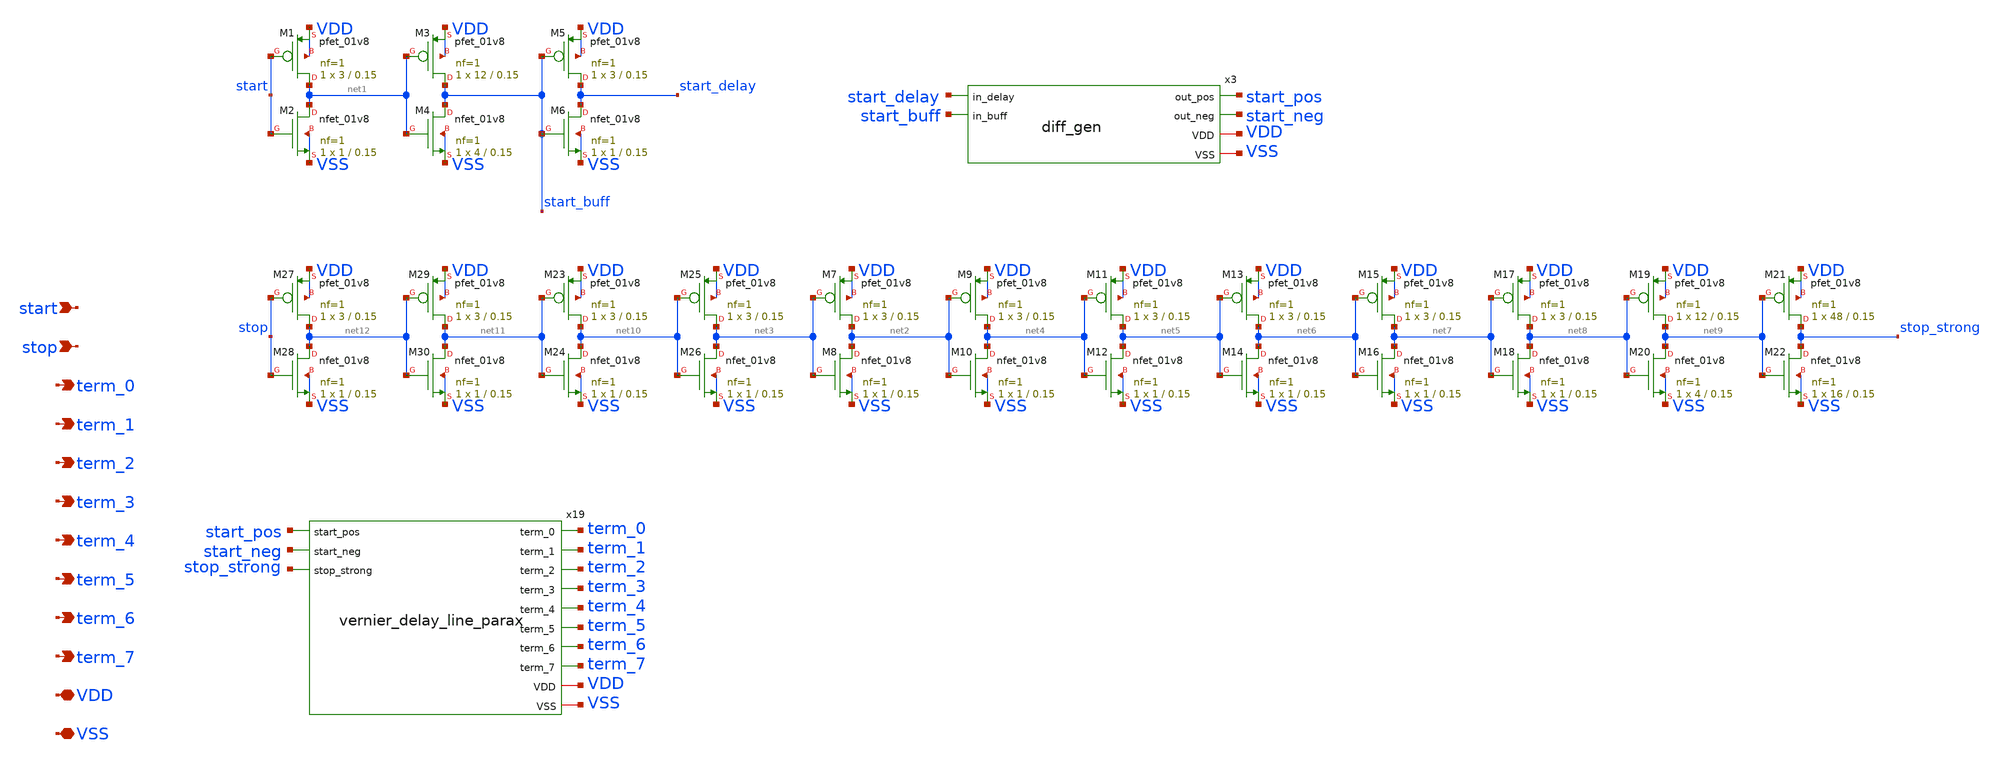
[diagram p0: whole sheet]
** sch_path: xschem/tdc_vernier_delay_line_post_layout.sch
**.subckt tdc_vernier_delay_line_post_layout VDD VSS start stop term_0 term_1 term_2 term_3 term_4
*+ term_5 term_6 term_7
*.iopin VDD
*.iopin VSS
*.ipin start
*.ipin stop
*.opin term_0
*.opin term_1
*.opin term_2
*.opin term_3
*.opin term_4
*.opin term_5
*.opin term_6
*.opin term_7
x3 start_delay start_buff start_pos start_neg VDD VSS diff_gen
XM1 net1 start VDD VDD sky130_fd_pr__pfet_01v8 L=0.15 W=3 nf=1 ad='int((nf+1)/2) * W/nf * 0.29' as='int((nf+2)/2) * W/nf * 0.29'
+ pd='2*int((nf+1)/2) * (W/nf + 0.29)' ps='2*int((nf+2)/2) * (W/nf + 0.29)' nrd='0.29 / W' nrs='0.29 / W'
+ sa=0 sb=0 sd=0 mult=1 m=1
XM2 net1 start VSS VSS sky130_fd_pr__nfet_01v8 L=0.15 W=1 nf=1 ad='int((nf+1)/2) * W/nf * 0.29' as='int((nf+2)/2) * W/nf * 0.29'
+ pd='2*int((nf+1)/2) * (W/nf + 0.29)' ps='2*int((nf+2)/2) * (W/nf + 0.29)' nrd='0.29 / W' nrs='0.29 / W'
+ sa=0 sb=0 sd=0 mult=1 m=1
XM3 start_buff net1 VDD VDD sky130_fd_pr__pfet_01v8 L=0.15 W=12 nf=1 ad='int((nf+1)/2) * W/nf * 0.29'
+ as='int((nf+2)/2) * W/nf * 0.29' pd='2*int((nf+1)/2) * (W/nf + 0.29)' ps='2*int((nf+2)/2) * (W/nf + 0.29)'
+ nrd='0.29 / W' nrs='0.29 / W' sa=0 sb=0 sd=0 mult=1 m=1
XM4 start_buff net1 VSS VSS sky130_fd_pr__nfet_01v8 L=0.15 W=4 nf=1 ad='int((nf+1)/2) * W/nf * 0.29'
+ as='int((nf+2)/2) * W/nf * 0.29' pd='2*int((nf+1)/2) * (W/nf + 0.29)' ps='2*int((nf+2)/2) * (W/nf + 0.29)'
+ nrd='0.29 / W' nrs='0.29 / W' sa=0 sb=0 sd=0 mult=1 m=1
XM5 start_delay start_buff VDD VDD sky130_fd_pr__pfet_01v8 L=0.15 W=3 nf=1 ad='int((nf+1)/2) * W/nf * 0.29'
+ as='int((nf+2)/2) * W/nf * 0.29' pd='2*int((nf+1)/2) * (W/nf + 0.29)' ps='2*int((nf+2)/2) * (W/nf + 0.29)'
+ nrd='0.29 / W' nrs='0.29 / W' sa=0 sb=0 sd=0 mult=1 m=1
XM6 start_delay start_buff VSS VSS sky130_fd_pr__nfet_01v8 L=0.15 W=1 nf=1 ad='int((nf+1)/2) * W/nf * 0.29'
+ as='int((nf+2)/2) * W/nf * 0.29' pd='2*int((nf+1)/2) * (W/nf + 0.29)' ps='2*int((nf+2)/2) * (W/nf + 0.29)'
+ nrd='0.29 / W' nrs='0.29 / W' sa=0 sb=0 sd=0 mult=1 m=1
XM7 net2 net3 VDD VDD sky130_fd_pr__pfet_01v8 L=0.15 W=3 nf=1 ad='int((nf+1)/2) * W/nf * 0.29' as='int((nf+2)/2) * W/nf * 0.29'
+ pd='2*int((nf+1)/2) * (W/nf + 0.29)' ps='2*int((nf+2)/2) * (W/nf + 0.29)' nrd='0.29 / W' nrs='0.29 / W'
+ sa=0 sb=0 sd=0 mult=1 m=1
XM8 net2 net3 VSS VSS sky130_fd_pr__nfet_01v8 L=0.15 W=1 nf=1 ad='int((nf+1)/2) * W/nf * 0.29' as='int((nf+2)/2) * W/nf * 0.29'
+ pd='2*int((nf+1)/2) * (W/nf + 0.29)' ps='2*int((nf+2)/2) * (W/nf + 0.29)' nrd='0.29 / W' nrs='0.29 / W'
+ sa=0 sb=0 sd=0 mult=1 m=1
XM9 net4 net2 VDD VDD sky130_fd_pr__pfet_01v8 L=0.15 W=3 nf=1 ad='int((nf+1)/2) * W/nf * 0.29' as='int((nf+2)/2) * W/nf * 0.29'
+ pd='2*int((nf+1)/2) * (W/nf + 0.29)' ps='2*int((nf+2)/2) * (W/nf + 0.29)' nrd='0.29 / W' nrs='0.29 / W'
+ sa=0 sb=0 sd=0 mult=1 m=1
XM10 net4 net2 VSS VSS sky130_fd_pr__nfet_01v8 L=0.15 W=1 nf=1 ad='int((nf+1)/2) * W/nf * 0.29' as='int((nf+2)/2) * W/nf * 0.29'
+ pd='2*int((nf+1)/2) * (W/nf + 0.29)' ps='2*int((nf+2)/2) * (W/nf + 0.29)' nrd='0.29 / W' nrs='0.29 / W'
+ sa=0 sb=0 sd=0 mult=1 m=1
XM11 net5 net4 VDD VDD sky130_fd_pr__pfet_01v8 L=0.15 W=3 nf=1 ad='int((nf+1)/2) * W/nf * 0.29' as='int((nf+2)/2) * W/nf * 0.29'
+ pd='2*int((nf+1)/2) * (W/nf + 0.29)' ps='2*int((nf+2)/2) * (W/nf + 0.29)' nrd='0.29 / W' nrs='0.29 / W'
+ sa=0 sb=0 sd=0 mult=1 m=1
XM12 net5 net4 VSS VSS sky130_fd_pr__nfet_01v8 L=0.15 W=1 nf=1 ad='int((nf+1)/2) * W/nf * 0.29' as='int((nf+2)/2) * W/nf * 0.29'
+ pd='2*int((nf+1)/2) * (W/nf + 0.29)' ps='2*int((nf+2)/2) * (W/nf + 0.29)' nrd='0.29 / W' nrs='0.29 / W'
+ sa=0 sb=0 sd=0 mult=1 m=1
XM13 net6 net5 VDD VDD sky130_fd_pr__pfet_01v8 L=0.15 W=3 nf=1 ad='int((nf+1)/2) * W/nf * 0.29' as='int((nf+2)/2) * W/nf * 0.29'
+ pd='2*int((nf+1)/2) * (W/nf + 0.29)' ps='2*int((nf+2)/2) * (W/nf + 0.29)' nrd='0.29 / W' nrs='0.29 / W'
+ sa=0 sb=0 sd=0 mult=1 m=1
XM14 net6 net5 VSS VSS sky130_fd_pr__nfet_01v8 L=0.15 W=1 nf=1 ad='int((nf+1)/2) * W/nf * 0.29' as='int((nf+2)/2) * W/nf * 0.29'
+ pd='2*int((nf+1)/2) * (W/nf + 0.29)' ps='2*int((nf+2)/2) * (W/nf + 0.29)' nrd='0.29 / W' nrs='0.29 / W'
+ sa=0 sb=0 sd=0 mult=1 m=1
XM15 net7 net6 VDD VDD sky130_fd_pr__pfet_01v8 L=0.15 W=3 nf=1 ad='int((nf+1)/2) * W/nf * 0.29' as='int((nf+2)/2) * W/nf * 0.29'
+ pd='2*int((nf+1)/2) * (W/nf + 0.29)' ps='2*int((nf+2)/2) * (W/nf + 0.29)' nrd='0.29 / W' nrs='0.29 / W'
+ sa=0 sb=0 sd=0 mult=1 m=1
XM16 net7 net6 VSS VSS sky130_fd_pr__nfet_01v8 L=0.15 W=1 nf=1 ad='int((nf+1)/2) * W/nf * 0.29' as='int((nf+2)/2) * W/nf * 0.29'
+ pd='2*int((nf+1)/2) * (W/nf + 0.29)' ps='2*int((nf+2)/2) * (W/nf + 0.29)' nrd='0.29 / W' nrs='0.29 / W'
+ sa=0 sb=0 sd=0 mult=1 m=1
XM17 net8 net7 VDD VDD sky130_fd_pr__pfet_01v8 L=0.15 W=3 nf=1 ad='int((nf+1)/2) * W/nf * 0.29' as='int((nf+2)/2) * W/nf * 0.29'
+ pd='2*int((nf+1)/2) * (W/nf + 0.29)' ps='2*int((nf+2)/2) * (W/nf + 0.29)' nrd='0.29 / W' nrs='0.29 / W'
+ sa=0 sb=0 sd=0 mult=1 m=1
XM18 net8 net7 VSS VSS sky130_fd_pr__nfet_01v8 L=0.15 W=1 nf=1 ad='int((nf+1)/2) * W/nf * 0.29' as='int((nf+2)/2) * W/nf * 0.29'
+ pd='2*int((nf+1)/2) * (W/nf + 0.29)' ps='2*int((nf+2)/2) * (W/nf + 0.29)' nrd='0.29 / W' nrs='0.29 / W'
+ sa=0 sb=0 sd=0 mult=1 m=1
XM19 net9 net8 VDD VDD sky130_fd_pr__pfet_01v8 L=0.15 W=12 nf=1 ad='int((nf+1)/2) * W/nf * 0.29' as='int((nf+2)/2) * W/nf * 0.29'
+ pd='2*int((nf+1)/2) * (W/nf + 0.29)' ps='2*int((nf+2)/2) * (W/nf + 0.29)' nrd='0.29 / W' nrs='0.29 / W'
+ sa=0 sb=0 sd=0 mult=1 m=1
XM20 net9 net8 VSS VSS sky130_fd_pr__nfet_01v8 L=0.15 W=4 nf=1 ad='int((nf+1)/2) * W/nf * 0.29' as='int((nf+2)/2) * W/nf * 0.29'
+ pd='2*int((nf+1)/2) * (W/nf + 0.29)' ps='2*int((nf+2)/2) * (W/nf + 0.29)' nrd='0.29 / W' nrs='0.29 / W'
+ sa=0 sb=0 sd=0 mult=1 m=1
XM21 stop_strong net9 VDD VDD sky130_fd_pr__pfet_01v8 L=0.15 W=48 nf=1 ad='int((nf+1)/2) * W/nf * 0.29'
+ as='int((nf+2)/2) * W/nf * 0.29' pd='2*int((nf+1)/2) * (W/nf + 0.29)' ps='2*int((nf+2)/2) * (W/nf + 0.29)'
+ nrd='0.29 / W' nrs='0.29 / W' sa=0 sb=0 sd=0 mult=1 m=1
XM22 stop_strong net9 VSS VSS sky130_fd_pr__nfet_01v8 L=0.15 W=16 nf=1 ad='int((nf+1)/2) * W/nf * 0.29'
+ as='int((nf+2)/2) * W/nf * 0.29' pd='2*int((nf+1)/2) * (W/nf + 0.29)' ps='2*int((nf+2)/2) * (W/nf + 0.29)'
+ nrd='0.29 / W' nrs='0.29 / W' sa=0 sb=0 sd=0 mult=1 m=1
XM23 net10 net11 VDD VDD sky130_fd_pr__pfet_01v8 L=0.15 W=3 nf=1 ad='int((nf+1)/2) * W/nf * 0.29' as='int((nf+2)/2) * W/nf * 0.29'
+ pd='2*int((nf+1)/2) * (W/nf + 0.29)' ps='2*int((nf+2)/2) * (W/nf + 0.29)' nrd='0.29 / W' nrs='0.29 / W'
+ sa=0 sb=0 sd=0 mult=1 m=1
XM24 net10 net11 VSS VSS sky130_fd_pr__nfet_01v8 L=0.15 W=1 nf=1 ad='int((nf+1)/2) * W/nf * 0.29' as='int((nf+2)/2) * W/nf * 0.29'
+ pd='2*int((nf+1)/2) * (W/nf + 0.29)' ps='2*int((nf+2)/2) * (W/nf + 0.29)' nrd='0.29 / W' nrs='0.29 / W'
+ sa=0 sb=0 sd=0 mult=1 m=1
XM25 net3 net10 VDD VDD sky130_fd_pr__pfet_01v8 L=0.15 W=3 nf=1 ad='int((nf+1)/2) * W/nf * 0.29' as='int((nf+2)/2) * W/nf * 0.29'
+ pd='2*int((nf+1)/2) * (W/nf + 0.29)' ps='2*int((nf+2)/2) * (W/nf + 0.29)' nrd='0.29 / W' nrs='0.29 / W'
+ sa=0 sb=0 sd=0 mult=1 m=1
XM26 net3 net10 VSS VSS sky130_fd_pr__nfet_01v8 L=0.15 W=1 nf=1 ad='int((nf+1)/2) * W/nf * 0.29' as='int((nf+2)/2) * W/nf * 0.29'
+ pd='2*int((nf+1)/2) * (W/nf + 0.29)' ps='2*int((nf+2)/2) * (W/nf + 0.29)' nrd='0.29 / W' nrs='0.29 / W'
+ sa=0 sb=0 sd=0 mult=1 m=1
XM27 net12 stop VDD VDD sky130_fd_pr__pfet_01v8 L=0.15 W=3 nf=1 ad='int((nf+1)/2) * W/nf * 0.29' as='int((nf+2)/2) * W/nf * 0.29'
+ pd='2*int((nf+1)/2) * (W/nf + 0.29)' ps='2*int((nf+2)/2) * (W/nf + 0.29)' nrd='0.29 / W' nrs='0.29 / W'
+ sa=0 sb=0 sd=0 mult=1 m=1
XM28 net12 stop VSS VSS sky130_fd_pr__nfet_01v8 L=0.15 W=1 nf=1 ad='int((nf+1)/2) * W/nf * 0.29' as='int((nf+2)/2) * W/nf * 0.29'
+ pd='2*int((nf+1)/2) * (W/nf + 0.29)' ps='2*int((nf+2)/2) * (W/nf + 0.29)' nrd='0.29 / W' nrs='0.29 / W'
+ sa=0 sb=0 sd=0 mult=1 m=1
XM29 net11 net12 VDD VDD sky130_fd_pr__pfet_01v8 L=0.15 W=3 nf=1 ad='int((nf+1)/2) * W/nf * 0.29' as='int((nf+2)/2) * W/nf * 0.29'
+ pd='2*int((nf+1)/2) * (W/nf + 0.29)' ps='2*int((nf+2)/2) * (W/nf + 0.29)' nrd='0.29 / W' nrs='0.29 / W'
+ sa=0 sb=0 sd=0 mult=1 m=1
XM30 net11 net12 VSS VSS sky130_fd_pr__nfet_01v8 L=0.15 W=1 nf=1 ad='int((nf+1)/2) * W/nf * 0.29' as='int((nf+2)/2) * W/nf * 0.29'
+ pd='2*int((nf+1)/2) * (W/nf + 0.29)' ps='2*int((nf+2)/2) * (W/nf + 0.29)' nrd='0.29 / W' nrs='0.29 / W'
+ sa=0 sb=0 sd=0 mult=1 m=1
x19 start_pos start_neg stop_strong term_0 term_1 term_2 term_3 term_4 term_5 term_6 term_7 VDD VSS
+ vernier_delay_line_parax
**.ends

* expanding   symbol:  diff_gen.sym # of pins=6
** sym_path: xschem/diff_gen.sym
** sch_path: xschem/diff_gen.sch
.subckt diff_gen in_delay in_buff out_pos out_neg VDD VSS
*.iopin VDD
*.iopin VSS
*.ipin in_delay
*.opin out_pos
*.ipin in_buff
*.opin out_neg
x1 out_1_1 in_delay out_2_1 in_buff VDD VSS phase_eq
x2 out_1_2 out_1_1 out_2_2 out_2_1 VDD VSS phase_eq
x3 out_1_3 out_1_2 out_2_3 out_2_2 VDD VSS phase_eq
x4 out_1_4 out_1_3 out_2_4 out_2_3 VDD VSS phase_eq
x5 out_1_5 out_1_4 out_2_5 out_2_4 VDD VSS phase_eq
x6 out_1_6 out_1_5 out_2_6 out_2_5 VDD VSS phase_eq
x7 out_pos out_1_6 out_neg out_2_6 VDD VSS phase_eq
.ends


* expanding   symbol:  vernier_delay_line_parax.sym # of pins=13
** sym_path: xschem/vernier_delay_line.sym
.include [file normalize ../mag/vernier_delay_line.sim.spice]

* expanding   symbol:  phase_eq.sym # of pins=6
** sym_path: xschem/phase_eq.sym
** sch_path: xschem/phase_eq.sch
.subckt phase_eq out_1 in_1 out_2 in_2 VDD VSS
*.iopin VDD
*.ipin in_1
*.opin out_1
*.iopin VSS
*.ipin in_2
*.opin out_2
XM5 out_1 in_1 VDD VDD sky130_fd_pr__pfet_01v8 L=0.15 W=9 nf=1 ad='int((nf+1)/2) * W/nf * 0.29' as='int((nf+2)/2) * W/nf * 0.29'
+ pd='2*int((nf+1)/2) * (W/nf + 0.29)' ps='2*int((nf+2)/2) * (W/nf + 0.29)' nrd='0.29 / W' nrs='0.29 / W'
+ sa=0 sb=0 sd=0 mult=1 m=1
XM7 out_1 in_1 VSS VSS sky130_fd_pr__nfet_01v8 L=0.15 W=3 nf=1 ad='int((nf+1)/2) * W/nf * 0.29' as='int((nf+2)/2) * W/nf * 0.29'
+ pd='2*int((nf+1)/2) * (W/nf + 0.29)' ps='2*int((nf+2)/2) * (W/nf + 0.29)' nrd='0.29 / W' nrs='0.29 / W'
+ sa=0 sb=0 sd=0 mult=1 m=1
XM1 out_2 in_2 VDD VDD sky130_fd_pr__pfet_01v8 L=0.15 W=9 nf=1 ad='int((nf+1)/2) * W/nf * 0.29' as='int((nf+2)/2) * W/nf * 0.29'
+ pd='2*int((nf+1)/2) * (W/nf + 0.29)' ps='2*int((nf+2)/2) * (W/nf + 0.29)' nrd='0.29 / W' nrs='0.29 / W'
+ sa=0 sb=0 sd=0 mult=1 m=1
XM2 out_2 in_2 VSS VSS sky130_fd_pr__nfet_01v8 L=0.15 W=3 nf=1 ad='int((nf+1)/2) * W/nf * 0.29' as='int((nf+2)/2) * W/nf * 0.29'
+ pd='2*int((nf+1)/2) * (W/nf + 0.29)' ps='2*int((nf+2)/2) * (W/nf + 0.29)' nrd='0.29 / W' nrs='0.29 / W'
+ sa=0 sb=0 sd=0 mult=1 m=1
XM3 in_1 in_2 VDD VDD sky130_fd_pr__pfet_01v8 L=0.15 W=3 nf=1 ad='int((nf+1)/2) * W/nf * 0.29' as='int((nf+2)/2) * W/nf * 0.29'
+ pd='2*int((nf+1)/2) * (W/nf + 0.29)' ps='2*int((nf+2)/2) * (W/nf + 0.29)' nrd='0.29 / W' nrs='0.29 / W'
+ sa=0 sb=0 sd=0 mult=1 m=1
XM4 in_1 in_2 VSS VSS sky130_fd_pr__nfet_01v8 L=0.15 W=1 nf=1 ad='int((nf+1)/2) * W/nf * 0.29' as='int((nf+2)/2) * W/nf * 0.29'
+ pd='2*int((nf+1)/2) * (W/nf + 0.29)' ps='2*int((nf+2)/2) * (W/nf + 0.29)' nrd='0.29 / W' nrs='0.29 / W'
+ sa=0 sb=0 sd=0 mult=1 m=1
XM6 in_2 in_1 VDD VDD sky130_fd_pr__pfet_01v8 L=0.15 W=3 nf=1 ad='int((nf+1)/2) * W/nf * 0.29' as='int((nf+2)/2) * W/nf * 0.29'
+ pd='2*int((nf+1)/2) * (W/nf + 0.29)' ps='2*int((nf+2)/2) * (W/nf + 0.29)' nrd='0.29 / W' nrs='0.29 / W'
+ sa=0 sb=0 sd=0 mult=1 m=1
XM8 in_2 in_1 VSS VSS sky130_fd_pr__nfet_01v8 L=0.15 W=1 nf=1 ad='int((nf+1)/2) * W/nf * 0.29' as='int((nf+2)/2) * W/nf * 0.29'
+ pd='2*int((nf+1)/2) * (W/nf + 0.29)' ps='2*int((nf+2)/2) * (W/nf + 0.29)' nrd='0.29 / W' nrs='0.29 / W'
+ sa=0 sb=0 sd=0 mult=1 m=1
.ends

.end
